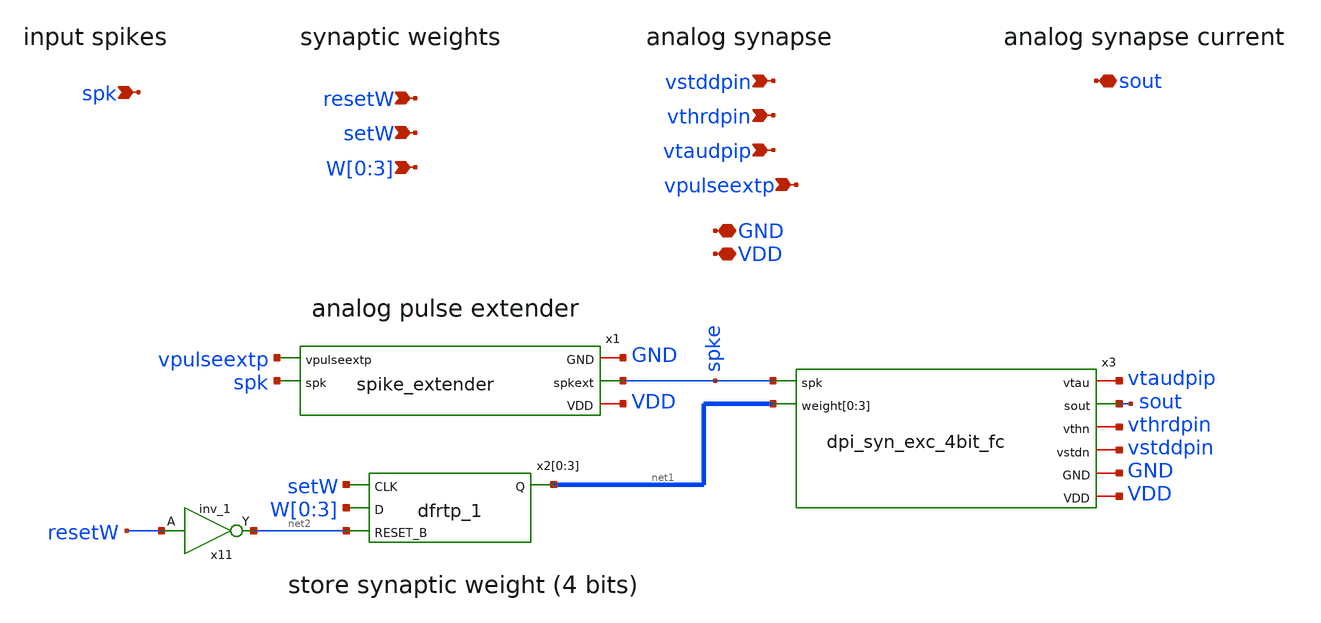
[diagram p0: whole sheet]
** sch_path: design/xschem/synapse_4bit_memory.sch
**.subckt synapse_4bit_memory GND VDD vpulseextp spk vthrdpin vtaudpip vstddpin W[0],W[1],W[2],W[3]
*+ setW resetW sout
*.iopin GND
*.iopin VDD
*.ipin vpulseextp
*.ipin spk
*.ipin vthrdpin
*.ipin vtaudpip
*.ipin vstddpin
*.ipin W[0],W[1],W[2],W[3]
*.ipin setW
*.ipin resetW
*.iopin sout
x1 vpulseextp spk GND spke VDD spike_extender
x3 vtaudpip sout vthrdpin spke vstddpin GND VDD net1[3] net1[2] net1[1] net1[0] dpi_syn_exc_4bit_fc
x2[0] setW W[0] net2 GND GND VDD VDD net1[3] sky130_fd_sc_hd__dfrtp_1
x2[1] setW W[1] net2 GND GND VDD VDD net1[2] sky130_fd_sc_hd__dfrtp_1
x2[2] setW W[2] net2 GND GND VDD VDD net1[1] sky130_fd_sc_hd__dfrtp_1
x2[3] setW W[3] net2 GND GND VDD VDD net1[0] sky130_fd_sc_hd__dfrtp_1
x11 resetW GND GND VDD VDD net2 sky130_fd_sc_hd__inv_1
**.ends

* expanding   symbol:  spike_extender.sym # of pins=5
** sym_path: design/xschem/spike_extender.sym
** sch_path: design/xschem/spike_extender.sch
.subckt spike_extender vpulseextp spk GND spkext VDD
*.iopin GND
*.iopin VDD
*.ipin spk
*.opin spkext
*.ipin vpulseextp
XM1 net1 spk GND GND sky130_fd_pr__nfet_01v8 L=0.15 W=0.65 nf=1 ad='int((nf+1)/2) * W/nf * 0.29' as='int((nf+2)/2) * W/nf * 0.29'
+ pd='2*int((nf+1)/2) * (W/nf + 0.29)' ps='2*int((nf+2)/2) * (W/nf + 0.29)' nrd='0.29 / W' nrs='0.29 / W'
+ sa=0 sb=0 sd=0 mult=1 m=1
XM6 net1 vpulseextp VDD VDD sky130_fd_pr__pfet_01v8 L=2 W=1 nf=1 ad='int((nf+1)/2) * W/nf * 0.29' as='int((nf+2)/2) * W/nf * 0.29'
+ pd='2*int((nf+1)/2) * (W/nf + 0.29)' ps='2*int((nf+2)/2) * (W/nf + 0.29)' nrd='0.29 / W' nrs='0.29 / W'
+ sa=0 sb=0 sd=0 mult=1 m=1
XM5 net3 net2 GND GND sky130_fd_pr__nfet_01v8 L=0.15 W=0.65 nf=1 ad='int((nf+1)/2) * W/nf * 0.29' as='int((nf+2)/2) * W/nf * 0.29'
+ pd='2*int((nf+1)/2) * (W/nf + 0.29)' ps='2*int((nf+2)/2) * (W/nf + 0.29)' nrd='0.29 / W' nrs='0.29 / W'
+ sa=0 sb=0 sd=0 mult=1 m=1
XM8 spkext net3 GND GND sky130_fd_pr__nfet_01v8 L=0.15 W=0.65 nf=1 ad='int((nf+1)/2) * W/nf * 0.29' as='int((nf+2)/2) * W/nf * 0.29'
+ pd='2*int((nf+1)/2) * (W/nf + 0.29)' ps='2*int((nf+2)/2) * (W/nf + 0.29)' nrd='0.29 / W' nrs='0.29 / W'
+ sa=0 sb=0 sd=0 mult=1 m=1
XM4 net3 net2 VDD VDD sky130_fd_pr__pfet_01v8 L=0.15 W=1.0 nf=1 ad='int((nf+1)/2) * W/nf * 0.29' as='int((nf+2)/2) * W/nf * 0.29'
+ pd='2*int((nf+1)/2) * (W/nf + 0.29)' ps='2*int((nf+2)/2) * (W/nf + 0.29)' nrd='0.29 / W' nrs='0.29 / W'
+ sa=0 sb=0 sd=0 mult=1 m=1
XM7 spkext net3 VDD VDD sky130_fd_pr__pfet_01v8 L=0.15 W=1.0 nf=1 ad='int((nf+1)/2) * W/nf * 0.29' as='int((nf+2)/2) * W/nf * 0.29'
+ pd='2*int((nf+1)/2) * (W/nf + 0.29)' ps='2*int((nf+2)/2) * (W/nf + 0.29)' nrd='0.29 / W' nrs='0.29 / W'
+ sa=0 sb=0 sd=0 mult=1 m=1
XM2 net2 net1 GND GND sky130_fd_pr__nfet_01v8 L=0.15 W=0.65 nf=1 ad='int((nf+1)/2) * W/nf * 0.29' as='int((nf+2)/2) * W/nf * 0.29'
+ pd='2*int((nf+1)/2) * (W/nf + 0.29)' ps='2*int((nf+2)/2) * (W/nf + 0.29)' nrd='0.29 / W' nrs='0.29 / W'
+ sa=0 sb=0 sd=0 mult=1 m=1
XM3 net2 net1 VDD VDD sky130_fd_pr__pfet_01v8 L=0.15 W=1.0 nf=1 ad='int((nf+1)/2) * W/nf * 0.29' as='int((nf+2)/2) * W/nf * 0.29'
+ pd='2*int((nf+1)/2) * (W/nf + 0.29)' ps='2*int((nf+2)/2) * (W/nf + 0.29)' nrd='0.29 / W' nrs='0.29 / W'
+ sa=0 sb=0 sd=0 mult=1 m=1
XM9 GND net1 GND GND sky130_fd_pr__nfet_01v8 L=1 W=0.65 nf=1 ad='int((nf+1)/2) * W/nf * 0.29' as='int((nf+2)/2) * W/nf * 0.29'
+ pd='2*int((nf+1)/2) * (W/nf + 0.29)' ps='2*int((nf+2)/2) * (W/nf + 0.29)' nrd='0.29 / W' nrs='0.29 / W'
+ sa=0 sb=0 sd=0 mult=1 m=1
.ends


* expanding   symbol:  dpi_syn_exc_4bit_fc.sym # of pins=8
** sym_path: design/xschem/dpi_syn_exc_4bit_fc.sym
** sch_path: design/xschem/dpi_syn_exc_4bit_fc.sch
.subckt dpi_syn_exc_4bit_fc vtau sout vthn spk vstdn GND VDD weight[0] weight[1] weight[2] weight[3]
*.iopin GND
*.iopin VDD
*.iopin vtau
*.iopin vstdn
*.ipin spk
*.opin sout
*.iopin vthn
*.ipin weight[0],weight[1],weight[2],weight[3]
XM2 net3 spk net1 GND sky130_fd_pr__nfet_01v8 L=0.25 W=0.8 nf=1 ad='int((nf+1)/2) * W/nf * 0.29' as='int((nf+2)/2) * W/nf * 0.29'
+ pd='2*int((nf+1)/2) * (W/nf + 0.29)' ps='2*int((nf+2)/2) * (W/nf + 0.29)' nrd='0.29 / W' nrs='0.29 / W'
+ sa=0 sb=0 sd=0 mult=1 m=1
XC1 vsin VDD sky130_fd_pr__cap_mim_m3_1 W=5 L=5 MF=1 m=1
XM5 vsin vtau VDD VDD sky130_fd_pr__pfet_01v8 L=0.2 W=1.2 nf=1 ad='int((nf+1)/2) * W/nf * 0.29' as='int((nf+2)/2) * W/nf * 0.29'
+ pd='2*int((nf+1)/2) * (W/nf + 0.29)' ps='2*int((nf+2)/2) * (W/nf + 0.29)' nrd='0.29 / W' nrs='0.29 / W'
+ sa=0 sb=0 sd=0 mult=1 m=1
XM6 sout vsin VDD VDD sky130_fd_pr__pfet_01v8 L=0.2 W=1.2 nf=1 ad='int((nf+1)/2) * W/nf * 0.29' as='int((nf+2)/2) * W/nf * 0.29'
+ pd='2*int((nf+1)/2) * (W/nf + 0.29)' ps='2*int((nf+2)/2) * (W/nf + 0.29)' nrd='0.29 / W' nrs='0.29 / W'
+ sa=0 sb=0 sd=0 mult=1 m=1
XM1 net1 vstdn net2 GND sky130_fd_pr__nfet_01v8 L=0.5 W=0.8 nf=1 ad='int((nf+1)/2) * W/nf * 0.29' as='int((nf+2)/2) * W/nf * 0.29'
+ pd='2*int((nf+1)/2) * (W/nf + 0.29)' ps='2*int((nf+2)/2) * (W/nf + 0.29)' nrd='0.29 / W' nrs='0.29 / W'
+ sa=0 sb=0 sd=0 mult=1 m=1
XM4 vsin vsin net3 GND sky130_fd_pr__nfet_01v8 L=0.25 W=0.8 nf=1 ad='int((nf+1)/2) * W/nf * 0.29' as='int((nf+2)/2) * W/nf * 0.29'
+ pd='2*int((nf+1)/2) * (W/nf + 0.29)' ps='2*int((nf+2)/2) * (W/nf + 0.29)' nrd='0.29 / W' nrs='0.29 / W'
+ sa=0 sb=0 sd=0 mult=1 m=1
XM3 VDD vthn net3 GND sky130_fd_pr__nfet_01v8 L=0.25 W=0.8 nf=1 ad='int((nf+1)/2) * W/nf * 0.29' as='int((nf+2)/2) * W/nf * 0.29'
+ pd='2*int((nf+1)/2) * (W/nf + 0.29)' ps='2*int((nf+2)/2) * (W/nf + 0.29)' nrd='0.29 / W' nrs='0.29 / W'
+ sa=0 sb=0 sd=0 mult=1 m=1
XM7 net1 vstdn net4 GND sky130_fd_pr__nfet_01v8 L=2.0 W=0.8 nf=1 ad='int((nf+1)/2) * W/nf * 0.29' as='int((nf+2)/2) * W/nf * 0.29'
+ pd='2*int((nf+1)/2) * (W/nf + 0.29)' ps='2*int((nf+2)/2) * (W/nf + 0.29)' nrd='0.29 / W' nrs='0.29 / W'
+ sa=0 sb=0 sd=0 mult=1 m=1
XM8 net1 vstdn net5 GND sky130_fd_pr__nfet_01v8 L=4.0 W=0.8 nf=1 ad='int((nf+1)/2) * W/nf * 0.29' as='int((nf+2)/2) * W/nf * 0.29'
+ pd='2*int((nf+1)/2) * (W/nf + 0.29)' ps='2*int((nf+2)/2) * (W/nf + 0.29)' nrd='0.29 / W' nrs='0.29 / W'
+ sa=0 sb=0 sd=0 mult=1 m=1
XM9 net1 vstdn net6 GND sky130_fd_pr__nfet_01v8 L=8.0 W=0.8 nf=1 ad='int((nf+1)/2) * W/nf * 0.29' as='int((nf+2)/2) * W/nf * 0.29'
+ pd='2*int((nf+1)/2) * (W/nf + 0.29)' ps='2*int((nf+2)/2) * (W/nf + 0.29)' nrd='0.29 / W' nrs='0.29 / W'
+ sa=0 sb=0 sd=0 mult=1 m=1
XM10 net2 weight[0] GND GND sky130_fd_pr__nfet_01v8 L=0.25 W=0.8 nf=1 ad='int((nf+1)/2) * W/nf * 0.29'
+ as='int((nf+2)/2) * W/nf * 0.29' pd='2*int((nf+1)/2) * (W/nf + 0.29)' ps='2*int((nf+2)/2) * (W/nf + 0.29)'
+ nrd='0.29 / W' nrs='0.29 / W' sa=0 sb=0 sd=0 mult=1 m=1
XM11 net4 weight[1] GND GND sky130_fd_pr__nfet_01v8 L=0.25 W=0.8 nf=1 ad='int((nf+1)/2) * W/nf * 0.29'
+ as='int((nf+2)/2) * W/nf * 0.29' pd='2*int((nf+1)/2) * (W/nf + 0.29)' ps='2*int((nf+2)/2) * (W/nf + 0.29)'
+ nrd='0.29 / W' nrs='0.29 / W' sa=0 sb=0 sd=0 mult=1 m=1
XM12 net5 weight[2] GND GND sky130_fd_pr__nfet_01v8 L=0.25 W=0.8 nf=1 ad='int((nf+1)/2) * W/nf * 0.29'
+ as='int((nf+2)/2) * W/nf * 0.29' pd='2*int((nf+1)/2) * (W/nf + 0.29)' ps='2*int((nf+2)/2) * (W/nf + 0.29)'
+ nrd='0.29 / W' nrs='0.29 / W' sa=0 sb=0 sd=0 mult=1 m=1
XM13 net6 weight[3] GND GND sky130_fd_pr__nfet_01v8 L=0.25 W=0.8 nf=1 ad='int((nf+1)/2) * W/nf * 0.29'
+ as='int((nf+2)/2) * W/nf * 0.29' pd='2*int((nf+1)/2) * (W/nf + 0.29)' ps='2*int((nf+2)/2) * (W/nf + 0.29)'
+ nrd='0.29 / W' nrs='0.29 / W' sa=0 sb=0 sd=0 mult=1 m=1
.ends

.end
